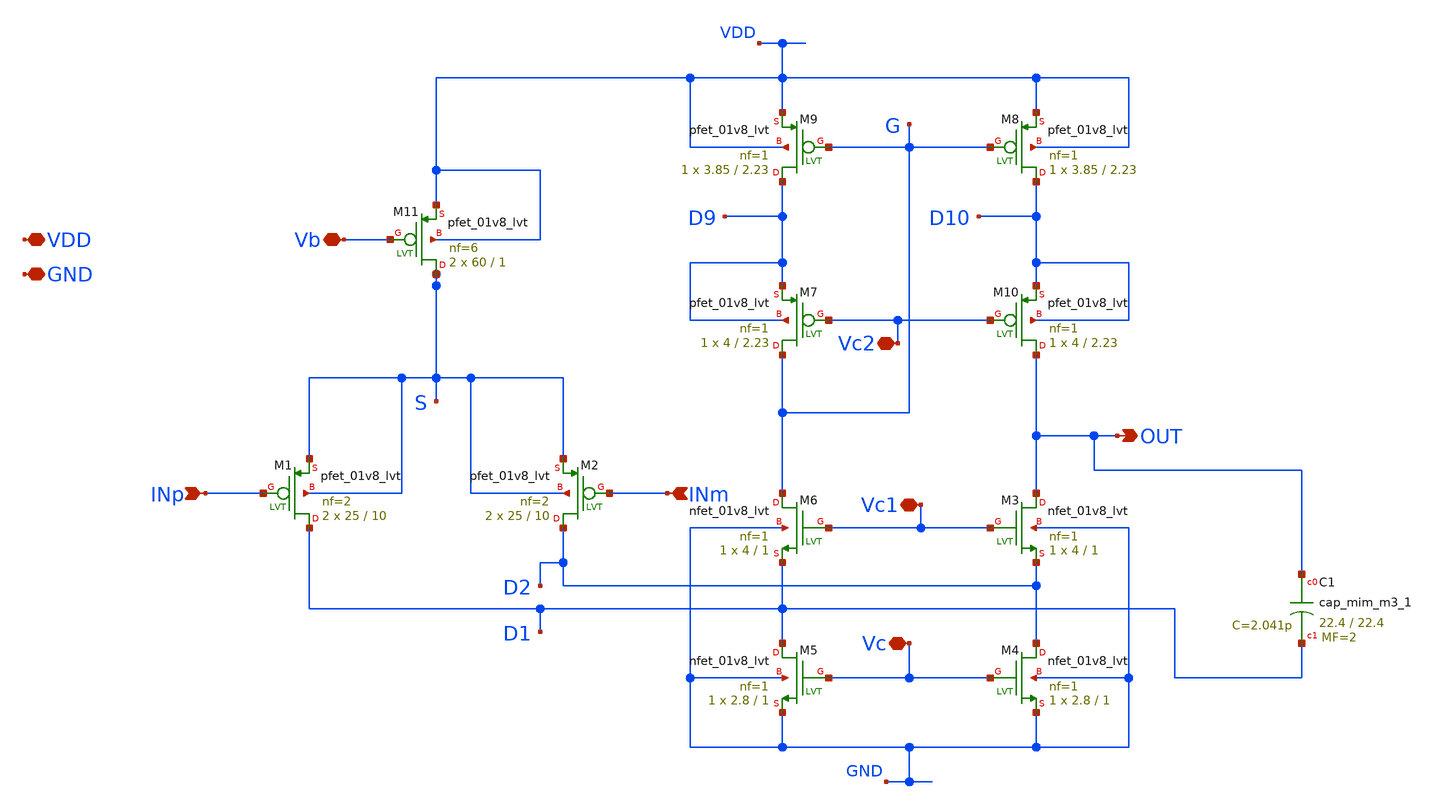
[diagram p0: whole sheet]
** sch_path: xschem/OFCB.sch
**.subckt OFCB VDD GND OUT INp INm Vc2 Vc1 Vc Vb
*.iopin VDD
*.iopin GND
*.opin OUT
*.ipin INp
*.ipin INm
*.iopin Vc2
*.iopin Vc1
*.iopin Vc
*.iopin Vb
XM11 S Vb VDD VDD sky130_fd_pr__pfet_01v8_lvt L=1 W=60 nf=6 ad='int((nf+1)/2) * W/nf * 0.29' as='int((nf+2)/2) * W/nf * 0.29'
+ pd='2*int((nf+1)/2) * (W/nf + 0.29)' ps='2*int((nf+2)/2) * (W/nf + 0.29)' nrd='0.29 / W' nrs='0.29 / W'
+ sa=0 sb=0 sd=0 mult=2 m=2
XM1 D1 INp S S sky130_fd_pr__pfet_01v8_lvt L=10 W=25 nf=2 ad='int((nf+1)/2) * W/nf * 0.29' as='int((nf+2)/2) * W/nf * 0.29'
+ pd='2*int((nf+1)/2) * (W/nf + 0.29)' ps='2*int((nf+2)/2) * (W/nf + 0.29)' nrd='0.29 / W' nrs='0.29 / W'
+ sa=0 sb=0 sd=0 mult=2 m=2
XM2 D2 INm S S sky130_fd_pr__pfet_01v8_lvt L=10 W=25 nf=2 ad='int((nf+1)/2) * W/nf * 0.29' as='int((nf+2)/2) * W/nf * 0.29'
+ pd='2*int((nf+1)/2) * (W/nf + 0.29)' ps='2*int((nf+2)/2) * (W/nf + 0.29)' nrd='0.29 / W' nrs='0.29 / W'
+ sa=0 sb=0 sd=0 mult=2 m=2
XM3 OUT Vc1 D2 GND sky130_fd_pr__nfet_01v8_lvt L=1 W=4 nf=1 ad='int((nf+1)/2) * W/nf * 0.29' as='int((nf+2)/2) * W/nf * 0.29'
+ pd='2*int((nf+1)/2) * (W/nf + 0.29)' ps='2*int((nf+2)/2) * (W/nf + 0.29)' nrd='0.29 / W' nrs='0.29 / W'
+ sa=0 sb=0 sd=0 mult=1 m=1
XM4 D2 Vc GND GND sky130_fd_pr__nfet_01v8_lvt L=1 W=2.8 nf=1 ad='int((nf+1)/2) * W/nf * 0.29' as='int((nf+2)/2) * W/nf * 0.29'
+ pd='2*int((nf+1)/2) * (W/nf + 0.29)' ps='2*int((nf+2)/2) * (W/nf + 0.29)' nrd='0.29 / W' nrs='0.29 / W'
+ sa=0 sb=0 sd=0 mult=1 m=1
XM5 D1 Vc GND GND sky130_fd_pr__nfet_01v8_lvt L=1 W=2.8 nf=1 ad='int((nf+1)/2) * W/nf * 0.29' as='int((nf+2)/2) * W/nf * 0.29'
+ pd='2*int((nf+1)/2) * (W/nf + 0.29)' ps='2*int((nf+2)/2) * (W/nf + 0.29)' nrd='0.29 / W' nrs='0.29 / W'
+ sa=0 sb=0 sd=0 mult=1 m=1
XM6 G Vc1 D1 GND sky130_fd_pr__nfet_01v8_lvt L=1 W=4 nf=1 ad='int((nf+1)/2) * W/nf * 0.29' as='int((nf+2)/2) * W/nf * 0.29'
+ pd='2*int((nf+1)/2) * (W/nf + 0.29)' ps='2*int((nf+2)/2) * (W/nf + 0.29)' nrd='0.29 / W' nrs='0.29 / W'
+ sa=0 sb=0 sd=0 mult=1 m=1
XM7 G Vc2 D9 D9 sky130_fd_pr__pfet_01v8_lvt L=2.23 W=4 nf=1 ad='int((nf+1)/2) * W/nf * 0.29' as='int((nf+2)/2) * W/nf * 0.29'
+ pd='2*int((nf+1)/2) * (W/nf + 0.29)' ps='2*int((nf+2)/2) * (W/nf + 0.29)' nrd='0.29 / W' nrs='0.29 / W'
+ sa=0 sb=0 sd=0 mult=1 m=1
XM9 D9 G VDD VDD sky130_fd_pr__pfet_01v8_lvt L=2.23 W=3.85 nf=1 ad='int((nf+1)/2) * W/nf * 0.29' as='int((nf+2)/2) * W/nf * 0.29'
+ pd='2*int((nf+1)/2) * (W/nf + 0.29)' ps='2*int((nf+2)/2) * (W/nf + 0.29)' nrd='0.29 / W' nrs='0.29 / W'
+ sa=0 sb=0 sd=0 mult=1 m=1
XM8 D10 G VDD VDD sky130_fd_pr__pfet_01v8_lvt L=2.23 W=3.85 nf=1 ad='int((nf+1)/2) * W/nf * 0.29' as='int((nf+2)/2) * W/nf * 0.29'
+ pd='2*int((nf+1)/2) * (W/nf + 0.29)' ps='2*int((nf+2)/2) * (W/nf + 0.29)' nrd='0.29 / W' nrs='0.29 / W'
+ sa=0 sb=0 sd=0 mult=1 m=1
XM10 OUT Vc2 D10 D10 sky130_fd_pr__pfet_01v8_lvt L=2.23 W=4 nf=1 ad='int((nf+1)/2) * W/nf * 0.29' as='int((nf+2)/2) * W/nf * 0.29'
+ pd='2*int((nf+1)/2) * (W/nf + 0.29)' ps='2*int((nf+2)/2) * (W/nf + 0.29)' nrd='0.29 / W' nrs='0.29 / W'
+ sa=0 sb=0 sd=0 mult=1 m=1
XC1 OUT D1 sky130_fd_pr__cap_mim_m3_1 W=22.4 L=22.4 MF=2 m=2
**.ends
.end
